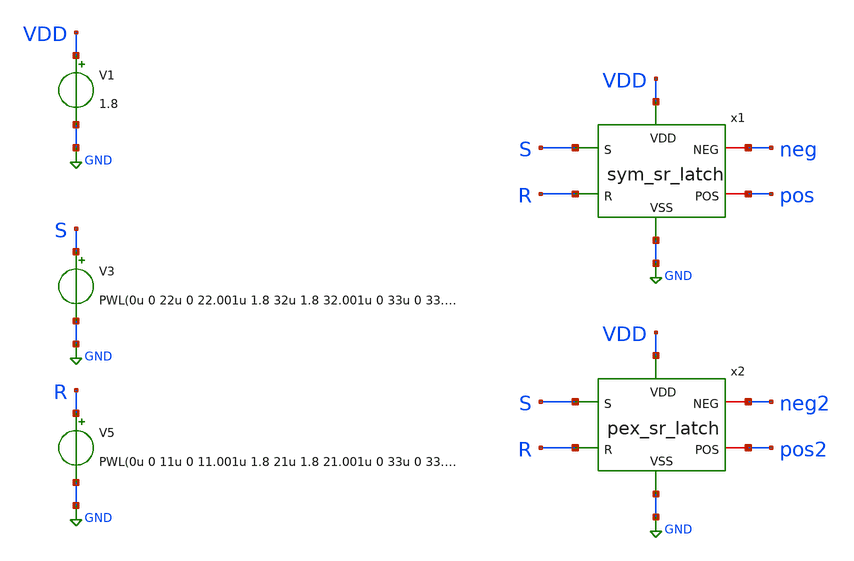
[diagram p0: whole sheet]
** sch_path: schem/tb/tb_sr_latch.sch
**.subckt tb_sr_latch
V1 VDD GND 1.8
V3 S GND PWL(0u 0 22u 0 22.001u 1.8 32u 1.8 32.001u 0 33u 0 33.001u 1.8 43u 1.8 43.001u 0 44u 0)
V5 R GND PWL(0u 0 11u 0 11.001u 1.8 21u 1.8 21.001u 0 33u 0 33.001u 1.8 43u 1.8 43.001u 0 44u 0)
x2 VDD GND R S neg2 pos2 sr_latch
x1 VDD GND R S neg pos sym_sr_latch
**** begin user architecture code


.include /home/zhixuan/projects/fyp_vco/magic/ip/sr_latch/sr_latch.spice
.lib /usr/local/share/pdk/sky130A/libs.tech/ngspice/sky130.lib.spice tt

.tran 10n 45u
.save all

.control
    run
    plot S R pos neg
.endc

.end


**** end user architecture code
**.ends

* expanding   symbol:  sym_sr_latch.sym # of pins=6
** sym_path: schem/symbol_repo/sym_sr_latch.sym
** sch_path: schem/symbol_repo/sym_sr_latch.sch
.subckt sym_sr_latch VDD VSS R S NEG POS
*.ipin S
*.ipin VDD
*.ipin R
*.ipin VSS
*.iopin POS
*.iopin NEG
XMN_neg POS NEG VSS VSS sky130_fd_pr__nfet_01v8 L=0.15 W=1 nf=1 ad='int((1 + 1)/2) * 1 / 1 * 0.29' as='int((1 + 2)/2) * 1 / 1 * 0.29'
+ pd='2*int((1 + 1)/2) * (1 / 1 + 0.29)' ps='2*int((1 + 2)/2) * (1 / 1 + 0.29)' nrd='0.29 / 1 ' nrs='0.29 / 1 '
+ sa=0 sb=0 sd=0 mult=1 m=1
XMP_s net1 S VDD VDD sky130_fd_pr__pfet_01v8 L=0.15 W=2 nf=1 ad='int((1 + 1)/2) * 2 / 1 * 0.29' as='int((1 + 2)/2) * 2 / 1 * 0.29'
+ pd='2*int((1 + 1)/2) * (2 / 1 + 0.29)' ps='2*int((1 + 2)/2) * (2 / 1 + 0.29)' nrd='0.29 / 2 ' nrs='0.29 / 2 '
+ sa=0 sb=0 sd=0 mult=1 m=1
XMP_neg POS NEG net1 VDD sky130_fd_pr__pfet_01v8 L=0.15 W=2 nf=1 ad='int((1 + 1)/2) * 2 / 1 * 0.29' as='int((1 + 2)/2) * 2 / 1 * 0.29'
+ pd='2*int((1 + 1)/2) * (2 / 1 + 0.29)' ps='2*int((1 + 2)/2) * (2 / 1 + 0.29)' nrd='0.29 / 2 ' nrs='0.29 / 2 '
+ sa=0 sb=0 sd=0 mult=1 m=1
XMN_s POS S VSS VSS sky130_fd_pr__nfet_01v8 L=0.15 W=1 nf=1 ad='int((1 + 1)/2) * 1 / 1 * 0.29' as='int((1 + 2)/2) * 1 / 1 * 0.29'
+ pd='2*int((1 + 1)/2) * (1 / 1 + 0.29)' ps='2*int((1 + 2)/2) * (1 / 1 + 0.29)' nrd='0.29 / 1 ' nrs='0.29 / 1 '
+ sa=0 sb=0 sd=0 mult=1 m=1
XMN_r NEG R VSS VSS sky130_fd_pr__nfet_01v8 L=0.15 W=1 nf=1 ad='int((1 + 1)/2) * 1 / 1 * 0.29' as='int((1 + 2)/2) * 1 / 1 * 0.29'
+ pd='2*int((1 + 1)/2) * (1 / 1 + 0.29)' ps='2*int((1 + 2)/2) * (1 / 1 + 0.29)' nrd='0.29 / 1 ' nrs='0.29 / 1 '
+ sa=0 sb=0 sd=0 mult=1 m=1
XMP_r net2 R VDD VDD sky130_fd_pr__pfet_01v8 L=0.15 W=2 nf=1 ad='int((1 + 1)/2) * 2 / 1 * 0.29' as='int((1 + 2)/2) * 2 / 1 * 0.29'
+ pd='2*int((1 + 1)/2) * (2 / 1 + 0.29)' ps='2*int((1 + 2)/2) * (2 / 1 + 0.29)' nrd='0.29 / 2 ' nrs='0.29 / 2 '
+ sa=0 sb=0 sd=0 mult=1 m=1
XMP_pos NEG POS net2 VDD sky130_fd_pr__pfet_01v8 L=0.15 W=2 nf=1 ad='int((1 + 1)/2) * 2 / 1 * 0.29' as='int((1 + 2)/2) * 2 / 1 * 0.29'
+ pd='2*int((1 + 1)/2) * (2 / 1 + 0.29)' ps='2*int((1 + 2)/2) * (2 / 1 + 0.29)' nrd='0.29 / 2 ' nrs='0.29 / 2 '
+ sa=0 sb=0 sd=0 mult=1 m=1
XMN_pos NEG POS VSS VSS sky130_fd_pr__nfet_01v8 L=0.15 W=1 nf=1 ad='int((1 + 1)/2) * 1 / 1 * 0.29' as='int((1 + 2)/2) * 1 / 1 * 0.29'
+ pd='2*int((1 + 1)/2) * (1 / 1 + 0.29)' ps='2*int((1 + 2)/2) * (1 / 1 + 0.29)' nrd='0.29 / 1 ' nrs='0.29 / 1 '
+ sa=0 sb=0 sd=0 mult=1 m=1
.ends

.GLOBAL GND
.end
